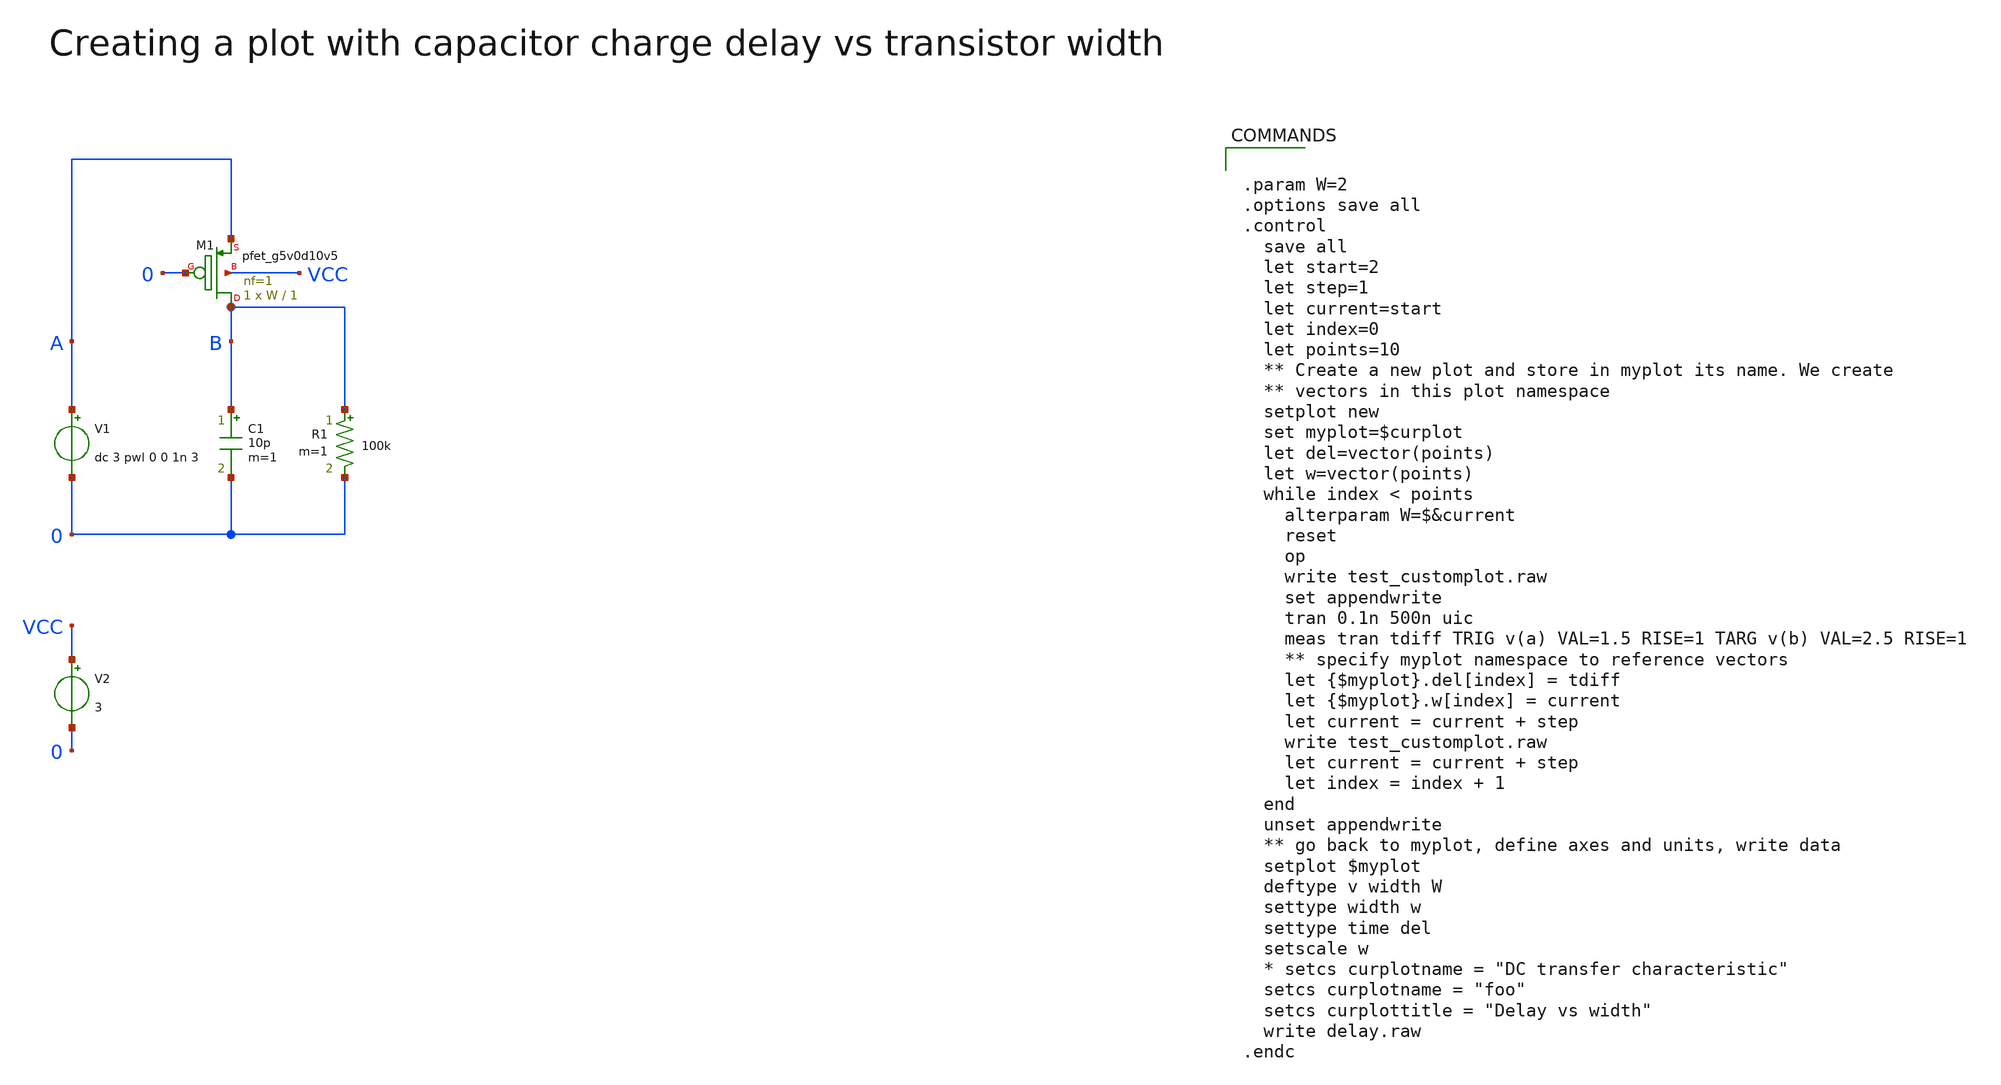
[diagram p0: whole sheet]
** sch_path: sky130A/xschem_libs/sky130_tests/test_customplot/schematic/test_customplot.sch
**.subckt test_customplot
V1 A 0 dc 3 pwl 0 0 1n 3
C1 B 0 10p m=1
XM1 B 0 A VCC sky130_fd_pr__pfet_g5v0d10v5 L=1 W=W nf=1 ad='int((1 + 1)/2) * W / 1 * 0.29' as='int((1 + 2)/2) * W / 1 * 0.29'
+ pd='2*int((1 + 1)/2) * (W / 1 + 0.29)' ps='2*int((1 + 2)/2) * (W / 1 + 0.29)' nrd='0.29 / W ' nrs='0.29 / W '
+ sa=0 sb=0 sd=0 mult=1 m=1
V2 VCC 0 3
R1 B 0 100k m=1
**** begin user architecture code


.param W=2
.options save all
.control
  save all
  let start=2
  let step=1
  let current=start
  let index=0
  let points=10
  ** Create a new plot and store in myplot its name. We create
  ** vectors in this plot namespace
  setplot new
  set myplot=$curplot
  let del=vector(points)
  let w=vector(points)
  while index < points
    alterparam W=$&current
    reset
    op
    write test_customplot.raw
    set appendwrite
    tran 0.1n 500n uic
    meas tran tdiff TRIG v(a) VAL=1.5 RISE=1 TARG v(b) VAL=2.5 RISE=1
    ** specify myplot namespace to reference vectors
    let {$myplot}.del[index] = tdiff
    let {$myplot}.w[index] = current
    let current = current + step
    write test_customplot.raw
    let current = current + step
    let index = index + 1
  end
  unset appendwrite
  ** go back to myplot, define axes and units, write data
  setplot $myplot
  deftype v width W
  settype width w
  settype time del
  setscale w
  * setcs curplotname = "DC transfer characteristic"
  setcs curplotname = "foo"
  setcs curplottitle = "Delay vs width"
  write delay.raw
.endc



** opencircuitdesign pdks install
.lib $::SKYWATER_MODELS/sky130.lib.spice tt

**** end user architecture code
**.ends
.end
